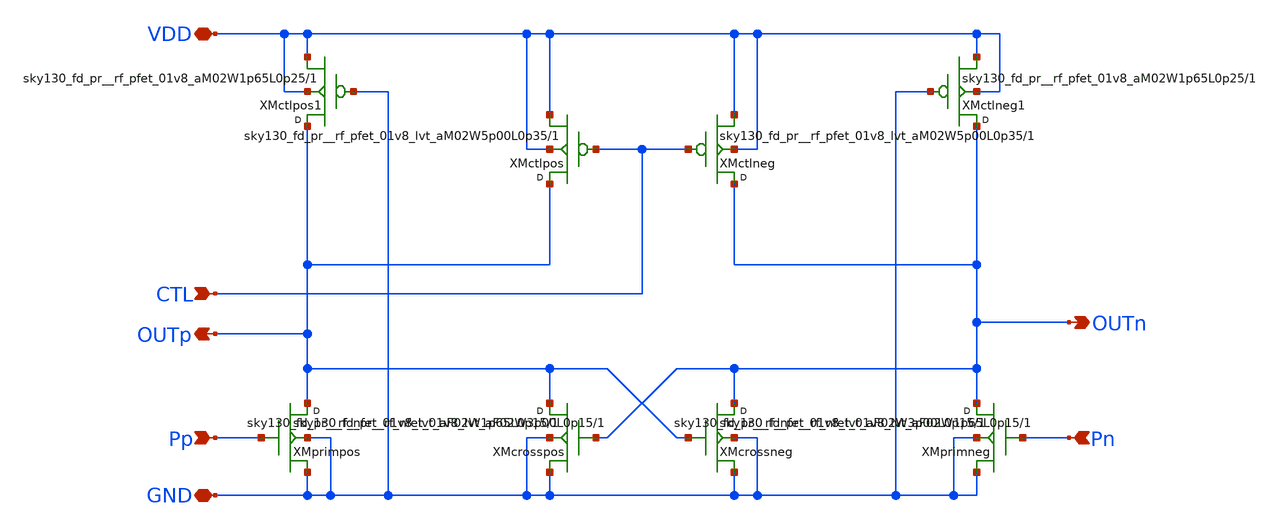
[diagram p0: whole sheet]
** sch_path: design/vco_2-4GHz_delaycell/vco_2-4GHz_delaycell.sch
**.subckt vco_2-4GHz_delaycell Pp Pn OUTn OUTp VDD GND CTL
*.ipin Pp
*.ipin Pn
*.opin OUTn
*.opin OUTp
*.iopin VDD
*.iopin GND
*.ipin CTL
XXMprimpos OUTp Pp GND GND sky130_fd_pr__rf_nfet_01v8_lvt_aF02W3p00L0p15 m=1
XXMcrossneg OUTn OUTp GND GND sky130_fd_pr__rf_nfet_01v8_lvt_aF02W1p65L0p15 m=1
XXMctlneg OUTn CTL VDD VDD sky130_fd_pr__rf_pfet_01v8_lvt_aM02W5p00L0p35 m=1
XXMctlpos OUTp CTL VDD VDD sky130_fd_pr__rf_pfet_01v8_lvt_aM02W5p00L0p35 m=1
XXMcrosspos OUTp OUTn GND GND sky130_fd_pr__rf_nfet_01v8_lvt_aF02W1p65L0p15 m=1
XXMprimneg OUTn Pn GND GND sky130_fd_pr__rf_nfet_01v8_lvt_aF02W3p00L0p15 m=1
XXMctlpos1 OUTp GND VDD VDD sky130_fd_pr__rf_pfet_01v8_aM02W1p65L0p25 m=1
XXMctlneg1 OUTn GND VDD VDD sky130_fd_pr__rf_pfet_01v8_aM02W1p65L0p25 m=1
**.ends
.end
